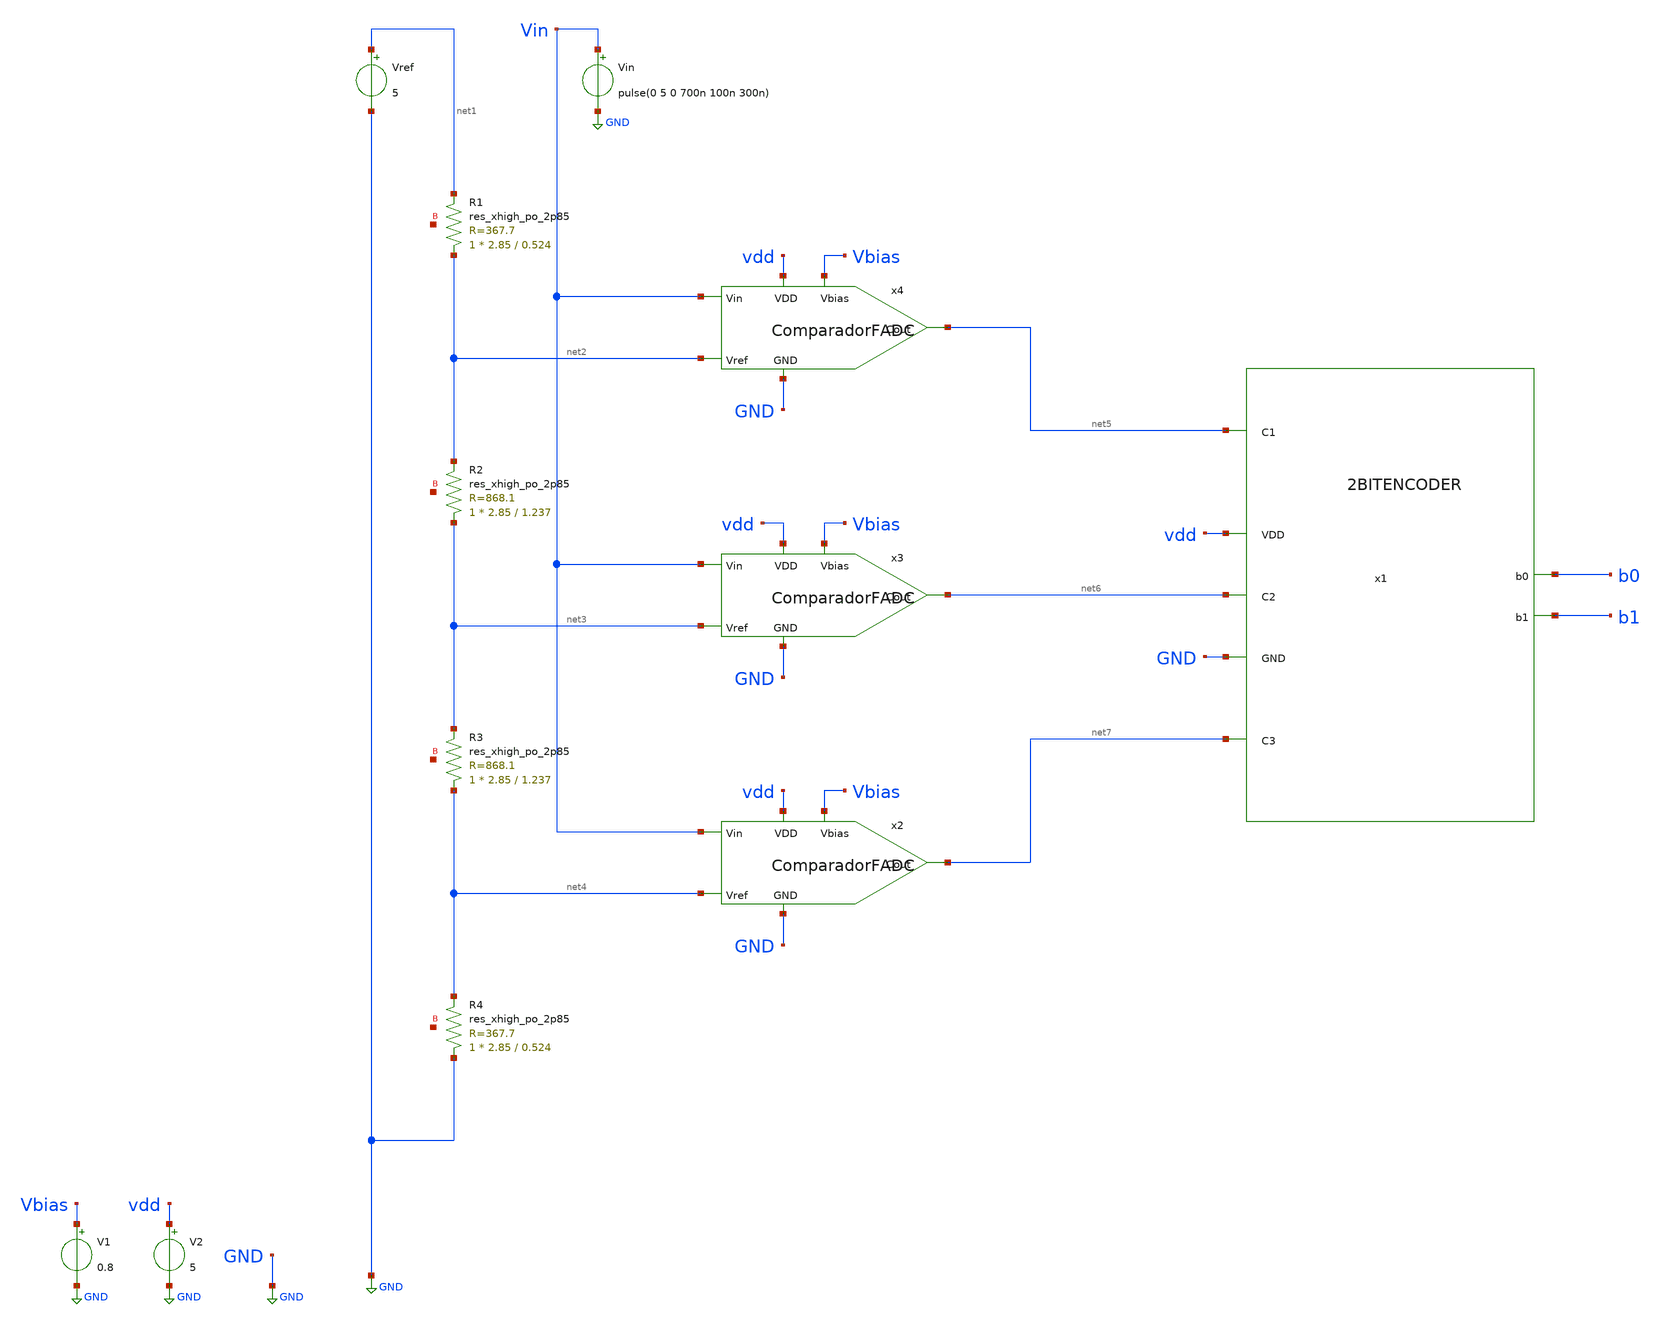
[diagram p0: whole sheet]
** sch_path: Analog Design Alan Rivera/Xschem/Sch/FinFlashadc.sch
**.subckt FinFlashadc
Vref net1 GND 5
Vin Vin GND pulse(0 5 0 700n 100n 300n)
V1 Vbias GND 0.8
V2 vdd GND 5
x1 net5 vdd GND b0 net6 b1 net7 2BITENCODER
x2 vdd Vin net4 net7 Vbias GND ComparadorFADC
x3 vdd Vin net3 net6 Vbias GND ComparadorFADC
x4 vdd Vin net2 net5 Vbias GND ComparadorFADC
XR1 net2 net1 net8 sky130_fd_pr__res_xhigh_po_2p85 L=0.524 mult=1 m=1
XR2 net3 net2 net9 sky130_fd_pr__res_xhigh_po_2p85 L=1.237 mult=1 m=1
XR3 net4 net3 net10 sky130_fd_pr__res_xhigh_po_2p85 L=1.237 mult=1 m=1
XR4 GND net4 net11 sky130_fd_pr__res_xhigh_po_2p85 L=0.524 mult=1 m=1
**** begin user architecture code


.lib /foss/pdks/sky130A/libs.tech/ngspice/sky130.lib.spice tt
.control
save all
*dc vin 0 5 0.05
tran 1n 3u
plot v(b0)
plot v(b1)


.endc


**** end user architecture code
**.ends
.GLOBAL GND
.end
